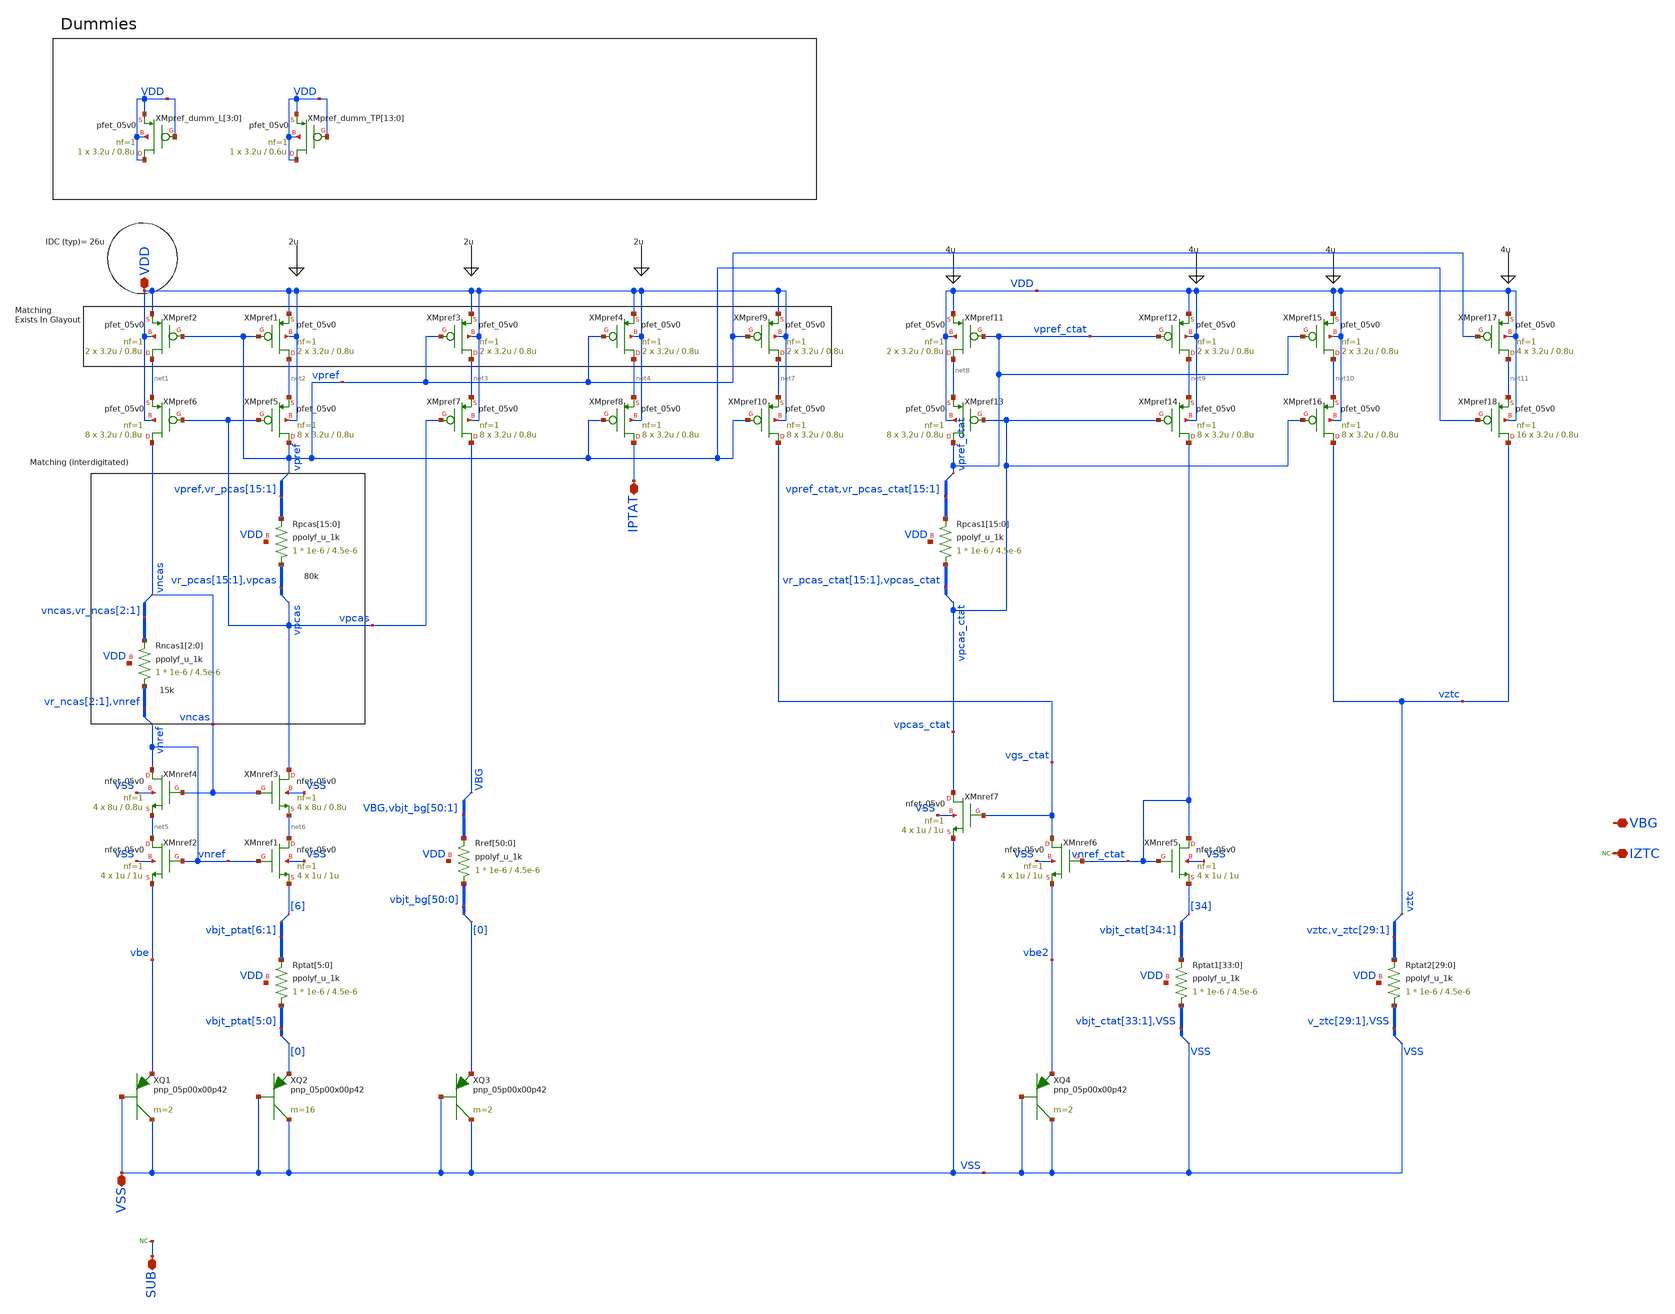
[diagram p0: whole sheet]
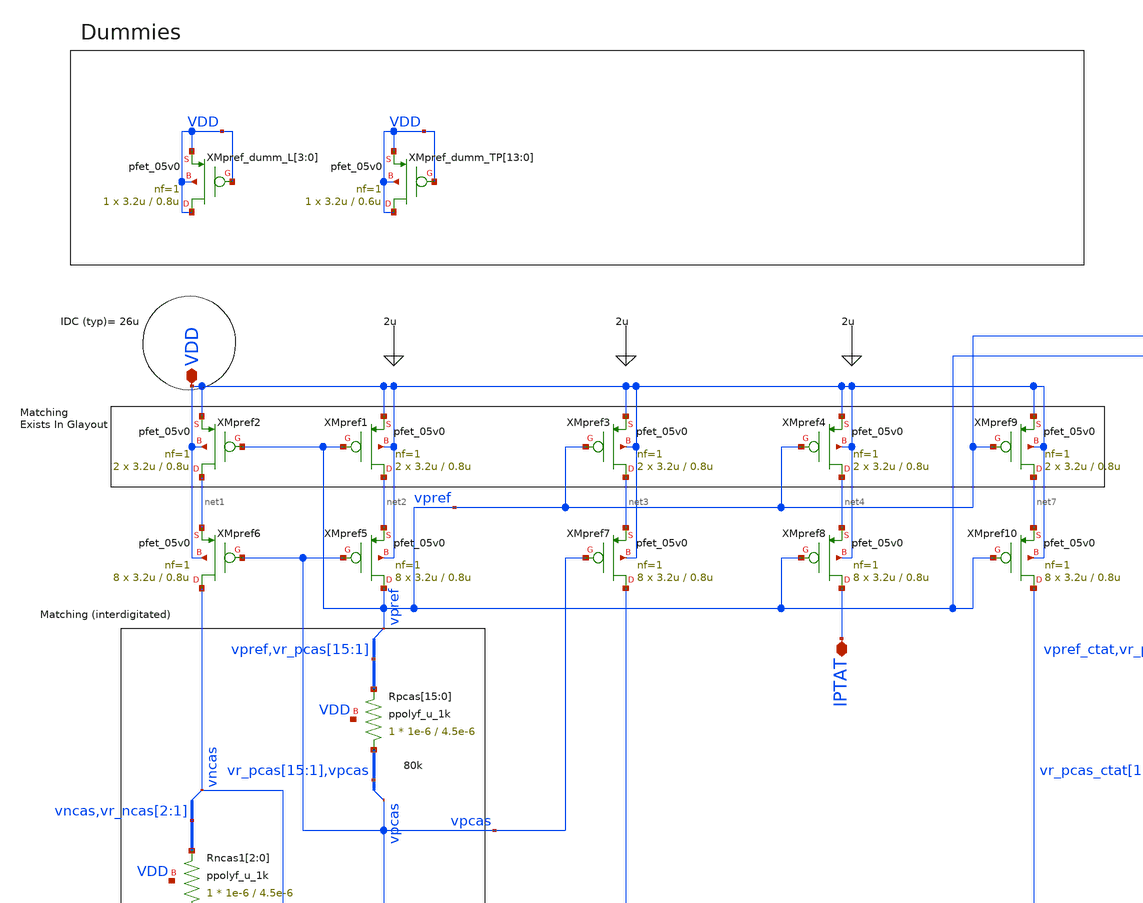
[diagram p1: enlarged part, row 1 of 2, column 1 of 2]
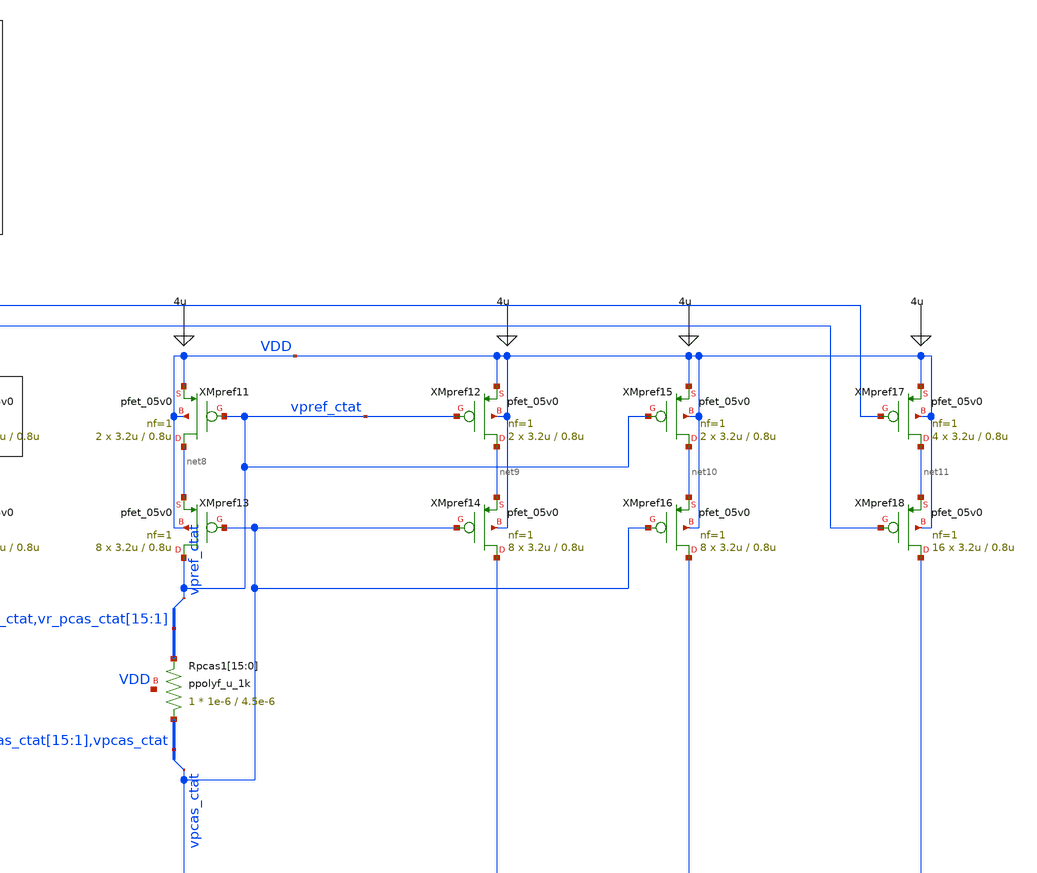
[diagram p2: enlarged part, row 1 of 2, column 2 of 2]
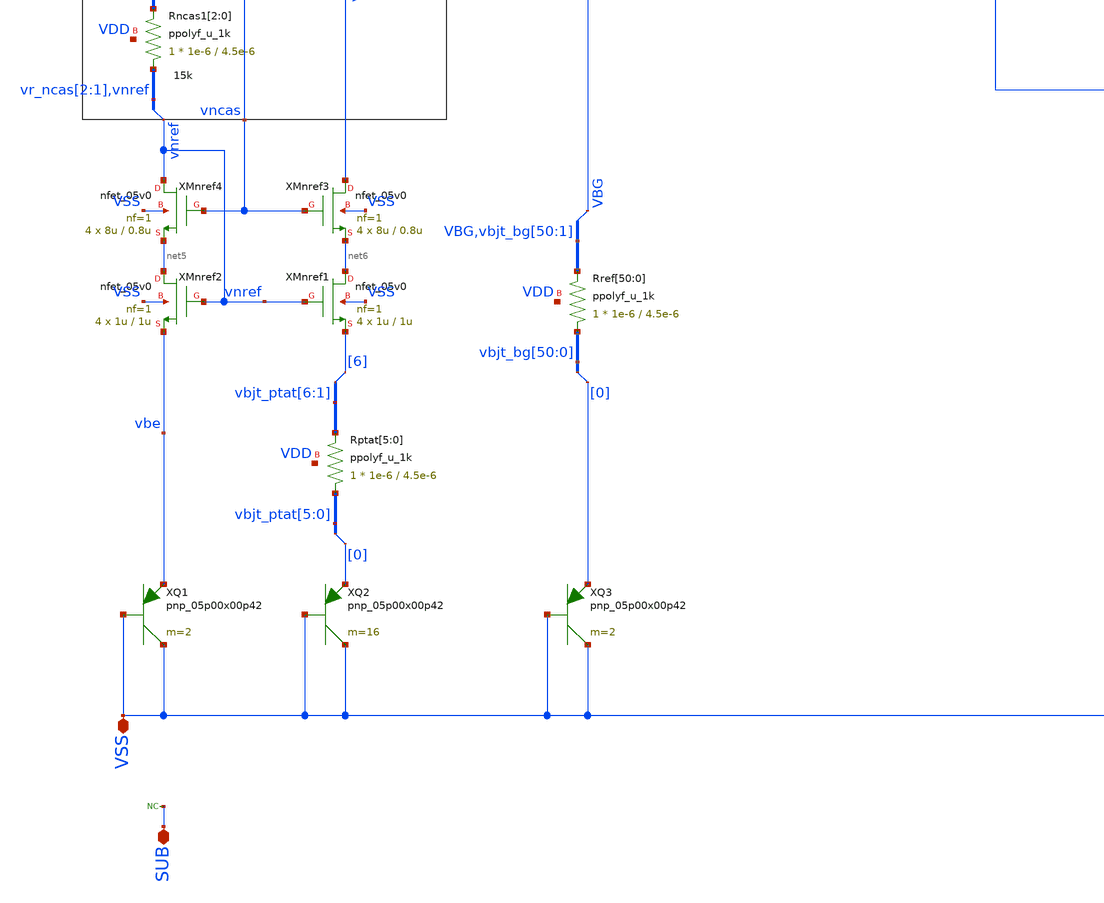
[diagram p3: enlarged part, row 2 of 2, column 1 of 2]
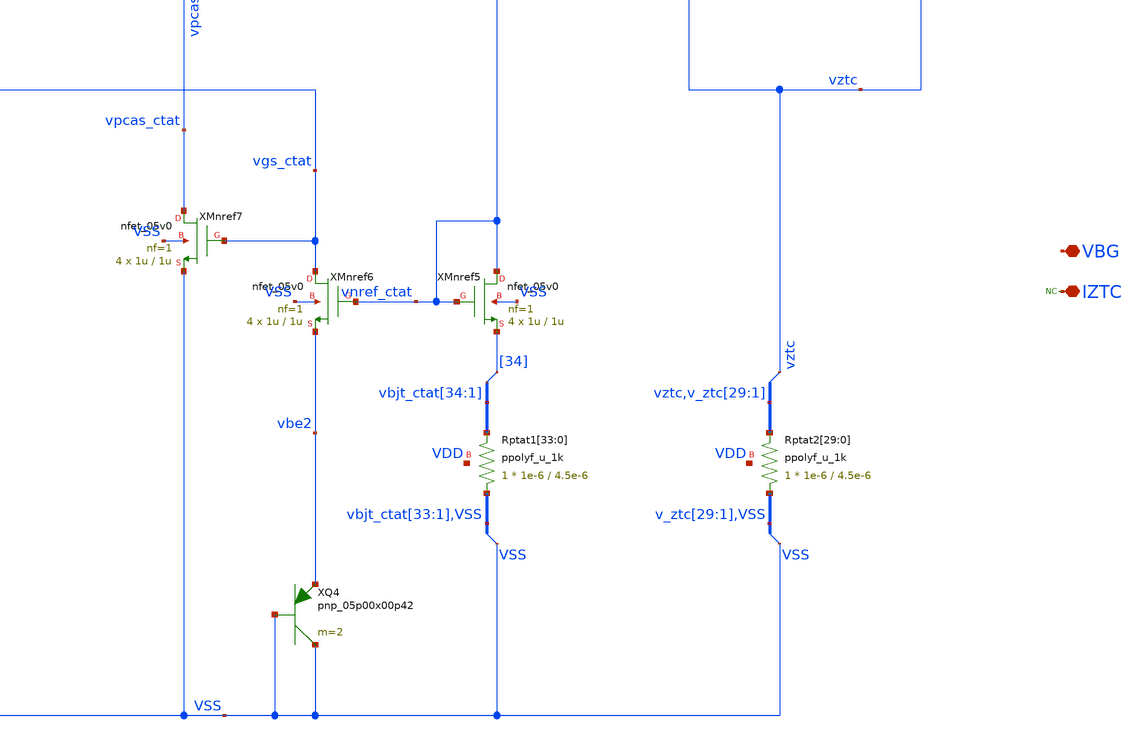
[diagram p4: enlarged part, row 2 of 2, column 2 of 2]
** sch_path: designs/libs/core_bandgap/bandgap/bandgap_no_opamp.sch
**.subckt bandgap_no_opamp VDD VSS SUB VBG IPTAT IZTC
*.iopin VDD
*.iopin VSS
*.iopin SUB
*.iopin VBG
*.iopin IPTAT
*.iopin IZTC
* noconn SUB
XQ1 VSS VSS vbe pnp_05p00x00p42 m=2 par=2
XQ2 VSS VSS vbjt_ptat[0] pnp_05p00x00p42 m=16 par=16
XMpref1 net2 vpref VDD VDD pfet_05v0 L=0.8u W=3.2u nf=1 ad='int((nf+1)/2) * W/nf * 0.18u' as='int((nf+2)/2) * W/nf * 0.18u'
+ pd='2*int((nf+1)/2) * (W/nf + 0.18u)' ps='2*int((nf+2)/2) * (W/nf + 0.18u)' nrd='0.18u / W' nrs='0.18u / W'
+ sa=0 sb=0 sd=0 m=2
XMnref1 net6 vnref vbjt_ptat[6] VSS nfet_05v0 L=1u W=1u nf=1 ad='int((nf+1)/2) * W/nf * 0.18u' as='int((nf+2)/2) * W/nf * 0.18u'
+ pd='2*int((nf+1)/2) * (W/nf + 0.18u)' ps='2*int((nf+2)/2) * (W/nf + 0.18u)' nrd='0.18u / W' nrs='0.18u / W'
+ sa=0 sb=0 sd=0 m=4
XMnref2 net5 vnref vbe VSS nfet_05v0 L=1u W=1u nf=1 ad='int((nf+1)/2) * W/nf * 0.18u' as='int((nf+2)/2) * W/nf * 0.18u'
+ pd='2*int((nf+1)/2) * (W/nf + 0.18u)' ps='2*int((nf+2)/2) * (W/nf + 0.18u)' nrd='0.18u / W' nrs='0.18u / W'
+ sa=0 sb=0 sd=0 m=4
XMpref2 net1 vpref VDD VDD pfet_05v0 L=0.8u W=3.2u nf=1 ad='int((nf+1)/2) * W/nf * 0.18u' as='int((nf+2)/2) * W/nf * 0.18u'
+ pd='2*int((nf+1)/2) * (W/nf + 0.18u)' ps='2*int((nf+2)/2) * (W/nf + 0.18u)' nrd='0.18u / W' nrs='0.18u / W'
+ sa=0 sb=0 sd=0 m=2
XRptat[5] vbjt_ptat[5] vbjt_ptat[6] VDD ppolyf_u_1k r_width=1e-6 r_length=4.5e-6 m=1
XRptat[4] vbjt_ptat[4] vbjt_ptat[5] VDD ppolyf_u_1k r_width=1e-6 r_length=4.5e-6 m=1
XRptat[3] vbjt_ptat[3] vbjt_ptat[4] VDD ppolyf_u_1k r_width=1e-6 r_length=4.5e-6 m=1
XRptat[2] vbjt_ptat[2] vbjt_ptat[3] VDD ppolyf_u_1k r_width=1e-6 r_length=4.5e-6 m=1
XRptat[1] vbjt_ptat[1] vbjt_ptat[2] VDD ppolyf_u_1k r_width=1e-6 r_length=4.5e-6 m=1
XRptat[0] vbjt_ptat[0] vbjt_ptat[1] VDD ppolyf_u_1k r_width=1e-6 r_length=4.5e-6 m=1
* tap: vbjt_ptat[5:0] --> vbjt_ptat[0]
* tap: vbjt_ptat[6:1] --> vbjt_ptat[6]
XQ3 VSS VSS vbjt_bg[0] pnp_05p00x00p42 m=2 par=2
XMpref3 net3 vpref VDD VDD pfet_05v0 L=0.8u W=3.2u nf=1 ad='int((nf+1)/2) * W/nf * 0.18u' as='int((nf+2)/2) * W/nf * 0.18u'
+ pd='2*int((nf+1)/2) * (W/nf + 0.18u)' ps='2*int((nf+2)/2) * (W/nf + 0.18u)' nrd='0.18u / W' nrs='0.18u / W'
+ sa=0 sb=0 sd=0 m=2
XRref[50] vbjt_bg[50] VBG VDD ppolyf_u_1k r_width=1e-6 r_length=4.5e-6 m=1
XRref[49] vbjt_bg[49] vbjt_bg[50] VDD ppolyf_u_1k r_width=1e-6 r_length=4.5e-6 m=1
XRref[48] vbjt_bg[48] vbjt_bg[49] VDD ppolyf_u_1k r_width=1e-6 r_length=4.5e-6 m=1
XRref[47] vbjt_bg[47] vbjt_bg[48] VDD ppolyf_u_1k r_width=1e-6 r_length=4.5e-6 m=1
XRref[46] vbjt_bg[46] vbjt_bg[47] VDD ppolyf_u_1k r_width=1e-6 r_length=4.5e-6 m=1
XRref[45] vbjt_bg[45] vbjt_bg[46] VDD ppolyf_u_1k r_width=1e-6 r_length=4.5e-6 m=1
XRref[44] vbjt_bg[44] vbjt_bg[45] VDD ppolyf_u_1k r_width=1e-6 r_length=4.5e-6 m=1
XRref[43] vbjt_bg[43] vbjt_bg[44] VDD ppolyf_u_1k r_width=1e-6 r_length=4.5e-6 m=1
XRref[42] vbjt_bg[42] vbjt_bg[43] VDD ppolyf_u_1k r_width=1e-6 r_length=4.5e-6 m=1
XRref[41] vbjt_bg[41] vbjt_bg[42] VDD ppolyf_u_1k r_width=1e-6 r_length=4.5e-6 m=1
XRref[40] vbjt_bg[40] vbjt_bg[41] VDD ppolyf_u_1k r_width=1e-6 r_length=4.5e-6 m=1
XRref[39] vbjt_bg[39] vbjt_bg[40] VDD ppolyf_u_1k r_width=1e-6 r_length=4.5e-6 m=1
XRref[38] vbjt_bg[38] vbjt_bg[39] VDD ppolyf_u_1k r_width=1e-6 r_length=4.5e-6 m=1
XRref[37] vbjt_bg[37] vbjt_bg[38] VDD ppolyf_u_1k r_width=1e-6 r_length=4.5e-6 m=1
XRref[36] vbjt_bg[36] vbjt_bg[37] VDD ppolyf_u_1k r_width=1e-6 r_length=4.5e-6 m=1
XRref[35] vbjt_bg[35] vbjt_bg[36] VDD ppolyf_u_1k r_width=1e-6 r_length=4.5e-6 m=1
XRref[34] vbjt_bg[34] vbjt_bg[35] VDD ppolyf_u_1k r_width=1e-6 r_length=4.5e-6 m=1
XRref[33] vbjt_bg[33] vbjt_bg[34] VDD ppolyf_u_1k r_width=1e-6 r_length=4.5e-6 m=1
XRref[32] vbjt_bg[32] vbjt_bg[33] VDD ppolyf_u_1k r_width=1e-6 r_length=4.5e-6 m=1
XRref[31] vbjt_bg[31] vbjt_bg[32] VDD ppolyf_u_1k r_width=1e-6 r_length=4.5e-6 m=1
XRref[30] vbjt_bg[30] vbjt_bg[31] VDD ppolyf_u_1k r_width=1e-6 r_length=4.5e-6 m=1
XRref[29] vbjt_bg[29] vbjt_bg[30] VDD ppolyf_u_1k r_width=1e-6 r_length=4.5e-6 m=1
XRref[28] vbjt_bg[28] vbjt_bg[29] VDD ppolyf_u_1k r_width=1e-6 r_length=4.5e-6 m=1
XRref[27] vbjt_bg[27] vbjt_bg[28] VDD ppolyf_u_1k r_width=1e-6 r_length=4.5e-6 m=1
XRref[26] vbjt_bg[26] vbjt_bg[27] VDD ppolyf_u_1k r_width=1e-6 r_length=4.5e-6 m=1
XRref[25] vbjt_bg[25] vbjt_bg[26] VDD ppolyf_u_1k r_width=1e-6 r_length=4.5e-6 m=1
XRref[24] vbjt_bg[24] vbjt_bg[25] VDD ppolyf_u_1k r_width=1e-6 r_length=4.5e-6 m=1
XRref[23] vbjt_bg[23] vbjt_bg[24] VDD ppolyf_u_1k r_width=1e-6 r_length=4.5e-6 m=1
XRref[22] vbjt_bg[22] vbjt_bg[23] VDD ppolyf_u_1k r_width=1e-6 r_length=4.5e-6 m=1
XRref[21] vbjt_bg[21] vbjt_bg[22] VDD ppolyf_u_1k r_width=1e-6 r_length=4.5e-6 m=1
XRref[20] vbjt_bg[20] vbjt_bg[21] VDD ppolyf_u_1k r_width=1e-6 r_length=4.5e-6 m=1
XRref[19] vbjt_bg[19] vbjt_bg[20] VDD ppolyf_u_1k r_width=1e-6 r_length=4.5e-6 m=1
XRref[18] vbjt_bg[18] vbjt_bg[19] VDD ppolyf_u_1k r_width=1e-6 r_length=4.5e-6 m=1
XRref[17] vbjt_bg[17] vbjt_bg[18] VDD ppolyf_u_1k r_width=1e-6 r_length=4.5e-6 m=1
XRref[16] vbjt_bg[16] vbjt_bg[17] VDD ppolyf_u_1k r_width=1e-6 r_length=4.5e-6 m=1
XRref[15] vbjt_bg[15] vbjt_bg[16] VDD ppolyf_u_1k r_width=1e-6 r_length=4.5e-6 m=1
XRref[14] vbjt_bg[14] vbjt_bg[15] VDD ppolyf_u_1k r_width=1e-6 r_length=4.5e-6 m=1
XRref[13] vbjt_bg[13] vbjt_bg[14] VDD ppolyf_u_1k r_width=1e-6 r_length=4.5e-6 m=1
XRref[12] vbjt_bg[12] vbjt_bg[13] VDD ppolyf_u_1k r_width=1e-6 r_length=4.5e-6 m=1
XRref[11] vbjt_bg[11] vbjt_bg[12] VDD ppolyf_u_1k r_width=1e-6 r_length=4.5e-6 m=1
XRref[10] vbjt_bg[10] vbjt_bg[11] VDD ppolyf_u_1k r_width=1e-6 r_length=4.5e-6 m=1
XRref[9] vbjt_bg[9] vbjt_bg[10] VDD ppolyf_u_1k r_width=1e-6 r_length=4.5e-6 m=1
XRref[8] vbjt_bg[8] vbjt_bg[9] VDD ppolyf_u_1k r_width=1e-6 r_length=4.5e-6 m=1
XRref[7] vbjt_bg[7] vbjt_bg[8] VDD ppolyf_u_1k r_width=1e-6 r_length=4.5e-6 m=1
XRref[6] vbjt_bg[6] vbjt_bg[7] VDD ppolyf_u_1k r_width=1e-6 r_length=4.5e-6 m=1
XRref[5] vbjt_bg[5] vbjt_bg[6] VDD ppolyf_u_1k r_width=1e-6 r_length=4.5e-6 m=1
XRref[4] vbjt_bg[4] vbjt_bg[5] VDD ppolyf_u_1k r_width=1e-6 r_length=4.5e-6 m=1
XRref[3] vbjt_bg[3] vbjt_bg[4] VDD ppolyf_u_1k r_width=1e-6 r_length=4.5e-6 m=1
XRref[2] vbjt_bg[2] vbjt_bg[3] VDD ppolyf_u_1k r_width=1e-6 r_length=4.5e-6 m=1
XRref[1] vbjt_bg[1] vbjt_bg[2] VDD ppolyf_u_1k r_width=1e-6 r_length=4.5e-6 m=1
XRref[0] vbjt_bg[0] vbjt_bg[1] VDD ppolyf_u_1k r_width=1e-6 r_length=4.5e-6 m=1
* tap: vbjt_bg[50:0] --> vbjt_bg[0]
XMpref4 net4 vpref VDD VDD pfet_05v0 L=0.8u W=3.2u nf=1 ad='int((nf+1)/2) * W/nf * 0.18u' as='int((nf+2)/2) * W/nf * 0.18u'
+ pd='2*int((nf+1)/2) * (W/nf + 0.18u)' ps='2*int((nf+2)/2) * (W/nf + 0.18u)' nrd='0.18u / W' nrs='0.18u / W'
+ sa=0 sb=0 sd=0 m=2
* noconn IZTC
XMpref5 vpref vpcas net2 VDD pfet_05v0 L=0.8u W=3.2u nf=1 ad='int((nf+1)/2) * W/nf * 0.18u' as='int((nf+2)/2) * W/nf * 0.18u'
+ pd='2*int((nf+1)/2) * (W/nf + 0.18u)' ps='2*int((nf+2)/2) * (W/nf + 0.18u)' nrd='0.18u / W' nrs='0.18u / W'
+ sa=0 sb=0 sd=0 m=8
XMpref6 vncas vpcas net1 VDD pfet_05v0 L=0.8u W=3.2u nf=1 ad='int((nf+1)/2) * W/nf * 0.18u' as='int((nf+2)/2) * W/nf * 0.18u'
+ pd='2*int((nf+1)/2) * (W/nf + 0.18u)' ps='2*int((nf+2)/2) * (W/nf + 0.18u)' nrd='0.18u / W' nrs='0.18u / W'
+ sa=0 sb=0 sd=0 m=8
XMpref7 VBG vpcas net3 VDD pfet_05v0 L=0.8u W=3.2u nf=1 ad='int((nf+1)/2) * W/nf * 0.18u' as='int((nf+2)/2) * W/nf * 0.18u'
+ pd='2*int((nf+1)/2) * (W/nf + 0.18u)' ps='2*int((nf+2)/2) * (W/nf + 0.18u)' nrd='0.18u / W' nrs='0.18u / W'
+ sa=0 sb=0 sd=0 m=8
XMpref8 IPTAT vpref net4 VDD pfet_05v0 L=0.8u W=3.2u nf=1 ad='int((nf+1)/2) * W/nf * 0.18u' as='int((nf+2)/2) * W/nf * 0.18u'
+ pd='2*int((nf+1)/2) * (W/nf + 0.18u)' ps='2*int((nf+2)/2) * (W/nf + 0.18u)' nrd='0.18u / W' nrs='0.18u / W'
+ sa=0 sb=0 sd=0 m=8
XRpcas[15] vr_pcas[15] vpref VDD ppolyf_u_1k r_width=1e-6 r_length=4.5e-6 m=1
XRpcas[14] vr_pcas[14] vr_pcas[15] VDD ppolyf_u_1k r_width=1e-6 r_length=4.5e-6 m=1
XRpcas[13] vr_pcas[13] vr_pcas[14] VDD ppolyf_u_1k r_width=1e-6 r_length=4.5e-6 m=1
XRpcas[12] vr_pcas[12] vr_pcas[13] VDD ppolyf_u_1k r_width=1e-6 r_length=4.5e-6 m=1
XRpcas[11] vr_pcas[11] vr_pcas[12] VDD ppolyf_u_1k r_width=1e-6 r_length=4.5e-6 m=1
XRpcas[10] vr_pcas[10] vr_pcas[11] VDD ppolyf_u_1k r_width=1e-6 r_length=4.5e-6 m=1
XRpcas[9] vr_pcas[9] vr_pcas[10] VDD ppolyf_u_1k r_width=1e-6 r_length=4.5e-6 m=1
XRpcas[8] vr_pcas[8] vr_pcas[9] VDD ppolyf_u_1k r_width=1e-6 r_length=4.5e-6 m=1
XRpcas[7] vr_pcas[7] vr_pcas[8] VDD ppolyf_u_1k r_width=1e-6 r_length=4.5e-6 m=1
XRpcas[6] vr_pcas[6] vr_pcas[7] VDD ppolyf_u_1k r_width=1e-6 r_length=4.5e-6 m=1
XRpcas[5] vr_pcas[5] vr_pcas[6] VDD ppolyf_u_1k r_width=1e-6 r_length=4.5e-6 m=1
XRpcas[4] vr_pcas[4] vr_pcas[5] VDD ppolyf_u_1k r_width=1e-6 r_length=4.5e-6 m=1
XRpcas[3] vr_pcas[3] vr_pcas[4] VDD ppolyf_u_1k r_width=1e-6 r_length=4.5e-6 m=1
XRpcas[2] vr_pcas[2] vr_pcas[3] VDD ppolyf_u_1k r_width=1e-6 r_length=4.5e-6 m=1
XRpcas[1] vr_pcas[1] vr_pcas[2] VDD ppolyf_u_1k r_width=1e-6 r_length=4.5e-6 m=1
XRpcas[0] vpcas vr_pcas[1] VDD ppolyf_u_1k r_width=1e-6 r_length=4.5e-6 m=1
XMnref3 vpcas vncas net6 VSS nfet_05v0 L=0.8u W=8u nf=1 ad='int((nf+1)/2) * W/nf * 0.18u' as='int((nf+2)/2) * W/nf * 0.18u'
+ pd='2*int((nf+1)/2) * (W/nf + 0.18u)' ps='2*int((nf+2)/2) * (W/nf + 0.18u)' nrd='0.18u / W' nrs='0.18u / W'
+ sa=0 sb=0 sd=0 m=4
XMnref4 vnref vncas net5 VSS nfet_05v0 L=0.8u W=8u nf=1 ad='int((nf+1)/2) * W/nf * 0.18u' as='int((nf+2)/2) * W/nf * 0.18u'
+ pd='2*int((nf+1)/2) * (W/nf + 0.18u)' ps='2*int((nf+2)/2) * (W/nf + 0.18u)' nrd='0.18u / W' nrs='0.18u / W'
+ sa=0 sb=0 sd=0 m=4
XRncas1[2] vr_ncas[2] vncas VDD ppolyf_u_1k r_width=1e-6 r_length=4.5e-6 m=1
XRncas1[1] vr_ncas[1] vr_ncas[2] VDD ppolyf_u_1k r_width=1e-6 r_length=4.5e-6 m=1
XRncas1[0] vnref vr_ncas[1] VDD ppolyf_u_1k r_width=1e-6 r_length=4.5e-6 m=1
XQ4 VSS VSS vbe2 pnp_05p00x00p42 m=2 par=2
XMnref5 vnref_ctat vnref_ctat vbjt_ctat[34] VSS nfet_05v0 L=1u W=1u nf=1 ad='int((nf+1)/2) * W/nf * 0.18u'
+ as='int((nf+2)/2) * W/nf * 0.18u' pd='2*int((nf+1)/2) * (W/nf + 0.18u)' ps='2*int((nf+2)/2) * (W/nf + 0.18u)'
+ nrd='0.18u / W' nrs='0.18u / W' sa=0 sb=0 sd=0 m=4
XMnref6 vgs_ctat vnref_ctat vbe2 VSS nfet_05v0 L=1u W=1u nf=1 ad='int((nf+1)/2) * W/nf * 0.18u' as='int((nf+2)/2) * W/nf * 0.18u'
+ pd='2*int((nf+1)/2) * (W/nf + 0.18u)' ps='2*int((nf+2)/2) * (W/nf + 0.18u)' nrd='0.18u / W' nrs='0.18u / W'
+ sa=0 sb=0 sd=0 m=4
XRptat1[33] vbjt_ctat[33] vbjt_ctat[34] VDD ppolyf_u_1k r_width=1e-6 r_length=4.5e-6 m=1
XRptat1[32] vbjt_ctat[32] vbjt_ctat[33] VDD ppolyf_u_1k r_width=1e-6 r_length=4.5e-6 m=1
XRptat1[31] vbjt_ctat[31] vbjt_ctat[32] VDD ppolyf_u_1k r_width=1e-6 r_length=4.5e-6 m=1
XRptat1[30] vbjt_ctat[30] vbjt_ctat[31] VDD ppolyf_u_1k r_width=1e-6 r_length=4.5e-6 m=1
XRptat1[29] vbjt_ctat[29] vbjt_ctat[30] VDD ppolyf_u_1k r_width=1e-6 r_length=4.5e-6 m=1
XRptat1[28] vbjt_ctat[28] vbjt_ctat[29] VDD ppolyf_u_1k r_width=1e-6 r_length=4.5e-6 m=1
XRptat1[27] vbjt_ctat[27] vbjt_ctat[28] VDD ppolyf_u_1k r_width=1e-6 r_length=4.5e-6 m=1
XRptat1[26] vbjt_ctat[26] vbjt_ctat[27] VDD ppolyf_u_1k r_width=1e-6 r_length=4.5e-6 m=1
XRptat1[25] vbjt_ctat[25] vbjt_ctat[26] VDD ppolyf_u_1k r_width=1e-6 r_length=4.5e-6 m=1
XRptat1[24] vbjt_ctat[24] vbjt_ctat[25] VDD ppolyf_u_1k r_width=1e-6 r_length=4.5e-6 m=1
XRptat1[23] vbjt_ctat[23] vbjt_ctat[24] VDD ppolyf_u_1k r_width=1e-6 r_length=4.5e-6 m=1
XRptat1[22] vbjt_ctat[22] vbjt_ctat[23] VDD ppolyf_u_1k r_width=1e-6 r_length=4.5e-6 m=1
XRptat1[21] vbjt_ctat[21] vbjt_ctat[22] VDD ppolyf_u_1k r_width=1e-6 r_length=4.5e-6 m=1
XRptat1[20] vbjt_ctat[20] vbjt_ctat[21] VDD ppolyf_u_1k r_width=1e-6 r_length=4.5e-6 m=1
XRptat1[19] vbjt_ctat[19] vbjt_ctat[20] VDD ppolyf_u_1k r_width=1e-6 r_length=4.5e-6 m=1
XRptat1[18] vbjt_ctat[18] vbjt_ctat[19] VDD ppolyf_u_1k r_width=1e-6 r_length=4.5e-6 m=1
XRptat1[17] vbjt_ctat[17] vbjt_ctat[18] VDD ppolyf_u_1k r_width=1e-6 r_length=4.5e-6 m=1
XRptat1[16] vbjt_ctat[16] vbjt_ctat[17] VDD ppolyf_u_1k r_width=1e-6 r_length=4.5e-6 m=1
XRptat1[15] vbjt_ctat[15] vbjt_ctat[16] VDD ppolyf_u_1k r_width=1e-6 r_length=4.5e-6 m=1
XRptat1[14] vbjt_ctat[14] vbjt_ctat[15] VDD ppolyf_u_1k r_width=1e-6 r_length=4.5e-6 m=1
XRptat1[13] vbjt_ctat[13] vbjt_ctat[14] VDD ppolyf_u_1k r_width=1e-6 r_length=4.5e-6 m=1
XRptat1[12] vbjt_ctat[12] vbjt_ctat[13] VDD ppolyf_u_1k r_width=1e-6 r_length=4.5e-6 m=1
XRptat1[11] vbjt_ctat[11] vbjt_ctat[12] VDD ppolyf_u_1k r_width=1e-6 r_length=4.5e-6 m=1
XRptat1[10] vbjt_ctat[10] vbjt_ctat[11] VDD ppolyf_u_1k r_width=1e-6 r_length=4.5e-6 m=1
XRptat1[9] vbjt_ctat[9] vbjt_ctat[10] VDD ppolyf_u_1k r_width=1e-6 r_length=4.5e-6 m=1
XRptat1[8] vbjt_ctat[8] vbjt_ctat[9] VDD ppolyf_u_1k r_width=1e-6 r_length=4.5e-6 m=1
XRptat1[7] vbjt_ctat[7] vbjt_ctat[8] VDD ppolyf_u_1k r_width=1e-6 r_length=4.5e-6 m=1
XRptat1[6] vbjt_ctat[6] vbjt_ctat[7] VDD ppolyf_u_1k r_width=1e-6 r_length=4.5e-6 m=1
XRptat1[5] vbjt_ctat[5] vbjt_ctat[6] VDD ppolyf_u_1k r_width=1e-6 r_length=4.5e-6 m=1
XRptat1[4] vbjt_ctat[4] vbjt_ctat[5] VDD ppolyf_u_1k r_width=1e-6 r_length=4.5e-6 m=1
XRptat1[3] vbjt_ctat[3] vbjt_ctat[4] VDD ppolyf_u_1k r_width=1e-6 r_length=4.5e-6 m=1
XRptat1[2] vbjt_ctat[2] vbjt_ctat[3] VDD ppolyf_u_1k r_width=1e-6 r_length=4.5e-6 m=1
XRptat1[1] vbjt_ctat[1] vbjt_ctat[2] VDD ppolyf_u_1k r_width=1e-6 r_length=4.5e-6 m=1
XRptat1[0] VSS vbjt_ctat[1] VDD ppolyf_u_1k r_width=1e-6 r_length=4.5e-6 m=1
* tap: vbjt_ctat[34:1] --> vbjt_ctat[34]
XMnref7 vpcas_ctat vgs_ctat VSS VSS nfet_05v0 L=1u W=1u nf=1 ad='int((nf+1)/2) * W/nf * 0.18u' as='int((nf+2)/2) * W/nf * 0.18u'
+ pd='2*int((nf+1)/2) * (W/nf + 0.18u)' ps='2*int((nf+2)/2) * (W/nf + 0.18u)' nrd='0.18u / W' nrs='0.18u / W'
+ sa=0 sb=0 sd=0 m=4
XMpref9 net7 vpref VDD VDD pfet_05v0 L=0.8u W=3.2u nf=1 ad='int((nf+1)/2) * W/nf * 0.18u' as='int((nf+2)/2) * W/nf * 0.18u'
+ pd='2*int((nf+1)/2) * (W/nf + 0.18u)' ps='2*int((nf+2)/2) * (W/nf + 0.18u)' nrd='0.18u / W' nrs='0.18u / W'
+ sa=0 sb=0 sd=0 m=2
XMpref10 vgs_ctat vpref net7 VDD pfet_05v0 L=0.8u W=3.2u nf=1 ad='int((nf+1)/2) * W/nf * 0.18u' as='int((nf+2)/2) * W/nf * 0.18u'
+ pd='2*int((nf+1)/2) * (W/nf + 0.18u)' ps='2*int((nf+2)/2) * (W/nf + 0.18u)' nrd='0.18u / W' nrs='0.18u / W'
+ sa=0 sb=0 sd=0 m=8
XMpref11 net8 vpref_ctat VDD VDD pfet_05v0 L=0.8u W=3.2u nf=1 ad='int((nf+1)/2) * W/nf * 0.18u' as='int((nf+2)/2) * W/nf * 0.18u'
+ pd='2*int((nf+1)/2) * (W/nf + 0.18u)' ps='2*int((nf+2)/2) * (W/nf + 0.18u)' nrd='0.18u / W' nrs='0.18u / W'
+ sa=0 sb=0 sd=0 m=2
XMpref12 net9 vpref_ctat VDD VDD pfet_05v0 L=0.8u W=3.2u nf=1 ad='int((nf+1)/2) * W/nf * 0.18u' as='int((nf+2)/2) * W/nf * 0.18u'
+ pd='2*int((nf+1)/2) * (W/nf + 0.18u)' ps='2*int((nf+2)/2) * (W/nf + 0.18u)' nrd='0.18u / W' nrs='0.18u / W'
+ sa=0 sb=0 sd=0 m=2
XRpcas1[15] vr_pcas_ctat[15] vpref_ctat VDD ppolyf_u_1k r_width=1e-6 r_length=4.5e-6 m=1
XRpcas1[14] vr_pcas_ctat[14] vr_pcas_ctat[15] VDD ppolyf_u_1k r_width=1e-6 r_length=4.5e-6 m=1
XRpcas1[13] vr_pcas_ctat[13] vr_pcas_ctat[14] VDD ppolyf_u_1k r_width=1e-6 r_length=4.5e-6 m=1
XRpcas1[12] vr_pcas_ctat[12] vr_pcas_ctat[13] VDD ppolyf_u_1k r_width=1e-6 r_length=4.5e-6 m=1
XRpcas1[11] vr_pcas_ctat[11] vr_pcas_ctat[12] VDD ppolyf_u_1k r_width=1e-6 r_length=4.5e-6 m=1
XRpcas1[10] vr_pcas_ctat[10] vr_pcas_ctat[11] VDD ppolyf_u_1k r_width=1e-6 r_length=4.5e-6 m=1
XRpcas1[9] vr_pcas_ctat[9] vr_pcas_ctat[10] VDD ppolyf_u_1k r_width=1e-6 r_length=4.5e-6 m=1
XRpcas1[8] vr_pcas_ctat[8] vr_pcas_ctat[9] VDD ppolyf_u_1k r_width=1e-6 r_length=4.5e-6 m=1
XRpcas1[7] vr_pcas_ctat[7] vr_pcas_ctat[8] VDD ppolyf_u_1k r_width=1e-6 r_length=4.5e-6 m=1
XRpcas1[6] vr_pcas_ctat[6] vr_pcas_ctat[7] VDD ppolyf_u_1k r_width=1e-6 r_length=4.5e-6 m=1
XRpcas1[5] vr_pcas_ctat[5] vr_pcas_ctat[6] VDD ppolyf_u_1k r_width=1e-6 r_length=4.5e-6 m=1
XRpcas1[4] vr_pcas_ctat[4] vr_pcas_ctat[5] VDD ppolyf_u_1k r_width=1e-6 r_length=4.5e-6 m=1
XRpcas1[3] vr_pcas_ctat[3] vr_pcas_ctat[4] VDD ppolyf_u_1k r_width=1e-6 r_length=4.5e-6 m=1
XRpcas1[2] vr_pcas_ctat[2] vr_pcas_ctat[3] VDD ppolyf_u_1k r_width=1e-6 r_length=4.5e-6 m=1
XRpcas1[1] vr_pcas_ctat[1] vr_pcas_ctat[2] VDD ppolyf_u_1k r_width=1e-6 r_length=4.5e-6 m=1
XRpcas1[0] vpcas_ctat vr_pcas_ctat[1] VDD ppolyf_u_1k r_width=1e-6 r_length=4.5e-6 m=1
XMpref13 vpref_ctat vpcas_ctat net8 VDD pfet_05v0 L=0.8u W=3.2u nf=1 ad='int((nf+1)/2) * W/nf * 0.18u'
+ as='int((nf+2)/2) * W/nf * 0.18u' pd='2*int((nf+1)/2) * (W/nf + 0.18u)' ps='2*int((nf+2)/2) * (W/nf + 0.18u)'
+ nrd='0.18u / W' nrs='0.18u / W' sa=0 sb=0 sd=0 m=8
XMpref14 vnref_ctat vpcas_ctat net9 VDD pfet_05v0 L=0.8u W=3.2u nf=1 ad='int((nf+1)/2) * W/nf * 0.18u'
+ as='int((nf+2)/2) * W/nf * 0.18u' pd='2*int((nf+1)/2) * (W/nf + 0.18u)' ps='2*int((nf+2)/2) * (W/nf + 0.18u)'
+ nrd='0.18u / W' nrs='0.18u / W' sa=0 sb=0 sd=0 m=8
XMpref15 net10 vpref_ctat VDD VDD pfet_05v0 L=0.8u W=3.2u nf=1 ad='int((nf+1)/2) * W/nf * 0.18u' as='int((nf+2)/2) * W/nf * 0.18u'
+ pd='2*int((nf+1)/2) * (W/nf + 0.18u)' ps='2*int((nf+2)/2) * (W/nf + 0.18u)' nrd='0.18u / W' nrs='0.18u / W'
+ sa=0 sb=0 sd=0 m=2
XMpref16 vztc vpcas_ctat net10 VDD pfet_05v0 L=0.8u W=3.2u nf=1 ad='int((nf+1)/2) * W/nf * 0.18u' as='int((nf+2)/2) * W/nf * 0.18u'
+ pd='2*int((nf+1)/2) * (W/nf + 0.18u)' ps='2*int((nf+2)/2) * (W/nf + 0.18u)' nrd='0.18u / W' nrs='0.18u / W'
+ sa=0 sb=0 sd=0 m=8
XRptat2[29] v_ztc[29] vztc VDD ppolyf_u_1k r_width=1e-6 r_length=4.5e-6 m=1
XRptat2[28] v_ztc[28] v_ztc[29] VDD ppolyf_u_1k r_width=1e-6 r_length=4.5e-6 m=1
XRptat2[27] v_ztc[27] v_ztc[28] VDD ppolyf_u_1k r_width=1e-6 r_length=4.5e-6 m=1
XRptat2[26] v_ztc[26] v_ztc[27] VDD ppolyf_u_1k r_width=1e-6 r_length=4.5e-6 m=1
XRptat2[25] v_ztc[25] v_ztc[26] VDD ppolyf_u_1k r_width=1e-6 r_length=4.5e-6 m=1
XRptat2[24] v_ztc[24] v_ztc[25] VDD ppolyf_u_1k r_width=1e-6 r_length=4.5e-6 m=1
XRptat2[23] v_ztc[23] v_ztc[24] VDD ppolyf_u_1k r_width=1e-6 r_length=4.5e-6 m=1
XRptat2[22] v_ztc[22] v_ztc[23] VDD ppolyf_u_1k r_width=1e-6 r_length=4.5e-6 m=1
XRptat2[21] v_ztc[21] v_ztc[22] VDD ppolyf_u_1k r_width=1e-6 r_length=4.5e-6 m=1
XRptat2[20] v_ztc[20] v_ztc[21] VDD ppolyf_u_1k r_width=1e-6 r_length=4.5e-6 m=1
XRptat2[19] v_ztc[19] v_ztc[20] VDD ppolyf_u_1k r_width=1e-6 r_length=4.5e-6 m=1
XRptat2[18] v_ztc[18] v_ztc[19] VDD ppolyf_u_1k r_width=1e-6 r_length=4.5e-6 m=1
XRptat2[17] v_ztc[17] v_ztc[18] VDD ppolyf_u_1k r_width=1e-6 r_length=4.5e-6 m=1
XRptat2[16] v_ztc[16] v_ztc[17] VDD ppolyf_u_1k r_width=1e-6 r_length=4.5e-6 m=1
XRptat2[15] v_ztc[15] v_ztc[16] VDD ppolyf_u_1k r_width=1e-6 r_length=4.5e-6 m=1
XRptat2[14] v_ztc[14] v_ztc[15] VDD ppolyf_u_1k r_width=1e-6 r_length=4.5e-6 m=1
XRptat2[13] v_ztc[13] v_ztc[14] VDD ppolyf_u_1k r_width=1e-6 r_length=4.5e-6 m=1
XRptat2[12] v_ztc[12] v_ztc[13] VDD ppolyf_u_1k r_width=1e-6 r_length=4.5e-6 m=1
XRptat2[11] v_ztc[11] v_ztc[12] VDD ppolyf_u_1k r_width=1e-6 r_length=4.5e-6 m=1
XRptat2[10] v_ztc[10] v_ztc[11] VDD ppolyf_u_1k r_width=1e-6 r_length=4.5e-6 m=1
XRptat2[9] v_ztc[9] v_ztc[10] VDD ppolyf_u_1k r_width=1e-6 r_length=4.5e-6 m=1
XRptat2[8] v_ztc[8] v_ztc[9] VDD ppolyf_u_1k r_width=1e-6 r_length=4.5e-6 m=1
XRptat2[7] v_ztc[7] v_ztc[8] VDD ppolyf_u_1k r_width=1e-6 r_length=4.5e-6 m=1
XRptat2[6] v_ztc[6] v_ztc[7] VDD ppolyf_u_1k r_width=1e-6 r_length=4.5e-6 m=1
XRptat2[5] v_ztc[5] v_ztc[6] VDD ppolyf_u_1k r_width=1e-6 r_length=4.5e-6 m=1
XRptat2[4] v_ztc[4] v_ztc[5] VDD ppolyf_u_1k r_width=1e-6 r_length=4.5e-6 m=1
XRptat2[3] v_ztc[3] v_ztc[4] VDD ppolyf_u_1k r_width=1e-6 r_length=4.5e-6 m=1
XRptat2[2] v_ztc[2] v_ztc[3] VDD ppolyf_u_1k r_width=1e-6 r_length=4.5e-6 m=1
XRptat2[1] v_ztc[1] v_ztc[2] VDD ppolyf_u_1k r_width=1e-6 r_length=4.5e-6 m=1
XRptat2[0] VSS v_ztc[1] VDD ppolyf_u_1k r_width=1e-6 r_length=4.5e-6 m=1
XMpref17 net11 vpref VDD VDD pfet_05v0 L=0.8u W=3.2u nf=1 ad='int((nf+1)/2) * W/nf * 0.18u' as='int((nf+2)/2) * W/nf * 0.18u'
+ pd='2*int((nf+1)/2) * (W/nf + 0.18u)' ps='2*int((nf+2)/2) * (W/nf + 0.18u)' nrd='0.18u / W' nrs='0.18u / W'
+ sa=0 sb=0 sd=0 m=4
XMpref18 vztc vpref net11 VDD pfet_05v0 L=0.8u W=3.2u nf=1 ad='int((nf+1)/2) * W/nf * 0.18u' as='int((nf+2)/2) * W/nf * 0.18u'
+ pd='2*int((nf+1)/2) * (W/nf + 0.18u)' ps='2*int((nf+2)/2) * (W/nf + 0.18u)' nrd='0.18u / W' nrs='0.18u / W'
+ sa=0 sb=0 sd=0 m=16
XMpref_dumm_L[3] VDD VDD VDD VDD pfet_05v0 L=0.8u W=3.2u nf=1 ad='int((nf+1)/2) * W/nf * 0.18u' as='int((nf+2)/2) * W/nf * 0.18u'
+ pd='2*int((nf+1)/2) * (W/nf + 0.18u)' ps='2*int((nf+2)/2) * (W/nf + 0.18u)' nrd='0.18u / W' nrs='0.18u / W'
+ sa=0 sb=0 sd=0 m=1
XMpref_dumm_L[2] VDD VDD VDD VDD pfet_05v0 L=0.8u W=3.2u nf=1 ad='int((nf+1)/2) * W/nf * 0.18u' as='int((nf+2)/2) * W/nf * 0.18u'
+ pd='2*int((nf+1)/2) * (W/nf + 0.18u)' ps='2*int((nf+2)/2) * (W/nf + 0.18u)' nrd='0.18u / W' nrs='0.18u / W'
+ sa=0 sb=0 sd=0 m=1
XMpref_dumm_L[1] VDD VDD VDD VDD pfet_05v0 L=0.8u W=3.2u nf=1 ad='int((nf+1)/2) * W/nf * 0.18u' as='int((nf+2)/2) * W/nf * 0.18u'
+ pd='2*int((nf+1)/2) * (W/nf + 0.18u)' ps='2*int((nf+2)/2) * (W/nf + 0.18u)' nrd='0.18u / W' nrs='0.18u / W'
+ sa=0 sb=0 sd=0 m=1
XMpref_dumm_L[0] VDD VDD VDD VDD pfet_05v0 L=0.8u W=3.2u nf=1 ad='int((nf+1)/2) * W/nf * 0.18u' as='int((nf+2)/2) * W/nf * 0.18u'
+ pd='2*int((nf+1)/2) * (W/nf + 0.18u)' ps='2*int((nf+2)/2) * (W/nf + 0.18u)' nrd='0.18u / W' nrs='0.18u / W'
+ sa=0 sb=0 sd=0 m=1
XMpref_dumm_TP[13] VDD VDD VDD VDD pfet_05v0 L=0.6u W=3.2u nf=1 ad='int((nf+1)/2) * W/nf * 0.18u' as='int((nf+2)/2) * W/nf * 0.18u'
+ pd='2*int((nf+1)/2) * (W/nf + 0.18u)' ps='2*int((nf+2)/2) * (W/nf + 0.18u)' nrd='0.18u / W' nrs='0.18u / W'
+ sa=0 sb=0 sd=0 m=1
XMpref_dumm_TP[12] VDD VDD VDD VDD pfet_05v0 L=0.6u W=3.2u nf=1 ad='int((nf+1)/2) * W/nf * 0.18u' as='int((nf+2)/2) * W/nf * 0.18u'
+ pd='2*int((nf+1)/2) * (W/nf + 0.18u)' ps='2*int((nf+2)/2) * (W/nf + 0.18u)' nrd='0.18u / W' nrs='0.18u / W'
+ sa=0 sb=0 sd=0 m=1
XMpref_dumm_TP[11] VDD VDD VDD VDD pfet_05v0 L=0.6u W=3.2u nf=1 ad='int((nf+1)/2) * W/nf * 0.18u' as='int((nf+2)/2) * W/nf * 0.18u'
+ pd='2*int((nf+1)/2) * (W/nf + 0.18u)' ps='2*int((nf+2)/2) * (W/nf + 0.18u)' nrd='0.18u / W' nrs='0.18u / W'
+ sa=0 sb=0 sd=0 m=1
XMpref_dumm_TP[10] VDD VDD VDD VDD pfet_05v0 L=0.6u W=3.2u nf=1 ad='int((nf+1)/2) * W/nf * 0.18u' as='int((nf+2)/2) * W/nf * 0.18u'
+ pd='2*int((nf+1)/2) * (W/nf + 0.18u)' ps='2*int((nf+2)/2) * (W/nf + 0.18u)' nrd='0.18u / W' nrs='0.18u / W'
+ sa=0 sb=0 sd=0 m=1
XMpref_dumm_TP[9] VDD VDD VDD VDD pfet_05v0 L=0.6u W=3.2u nf=1 ad='int((nf+1)/2) * W/nf * 0.18u' as='int((nf+2)/2) * W/nf * 0.18u'
+ pd='2*int((nf+1)/2) * (W/nf + 0.18u)' ps='2*int((nf+2)/2) * (W/nf + 0.18u)' nrd='0.18u / W' nrs='0.18u / W'
+ sa=0 sb=0 sd=0 m=1
XMpref_dumm_TP[8] VDD VDD VDD VDD pfet_05v0 L=0.6u W=3.2u nf=1 ad='int((nf+1)/2) * W/nf * 0.18u' as='int((nf+2)/2) * W/nf * 0.18u'
+ pd='2*int((nf+1)/2) * (W/nf + 0.18u)' ps='2*int((nf+2)/2) * (W/nf + 0.18u)' nrd='0.18u / W' nrs='0.18u / W'
+ sa=0 sb=0 sd=0 m=1
XMpref_dumm_TP[7] VDD VDD VDD VDD pfet_05v0 L=0.6u W=3.2u nf=1 ad='int((nf+1)/2) * W/nf * 0.18u' as='int((nf+2)/2) * W/nf * 0.18u'
+ pd='2*int((nf+1)/2) * (W/nf + 0.18u)' ps='2*int((nf+2)/2) * (W/nf + 0.18u)' nrd='0.18u / W' nrs='0.18u / W'
+ sa=0 sb=0 sd=0 m=1
XMpref_dumm_TP[6] VDD VDD VDD VDD pfet_05v0 L=0.6u W=3.2u nf=1 ad='int((nf+1)/2) * W/nf * 0.18u' as='int((nf+2)/2) * W/nf * 0.18u'
+ pd='2*int((nf+1)/2) * (W/nf + 0.18u)' ps='2*int((nf+2)/2) * (W/nf + 0.18u)' nrd='0.18u / W' nrs='0.18u / W'
+ sa=0 sb=0 sd=0 m=1
XMpref_dumm_TP[5] VDD VDD VDD VDD pfet_05v0 L=0.6u W=3.2u nf=1 ad='int((nf+1)/2) * W/nf * 0.18u' as='int((nf+2)/2) * W/nf * 0.18u'
+ pd='2*int((nf+1)/2) * (W/nf + 0.18u)' ps='2*int((nf+2)/2) * (W/nf + 0.18u)' nrd='0.18u / W' nrs='0.18u / W'
+ sa=0 sb=0 sd=0 m=1
XMpref_dumm_TP[4] VDD VDD VDD VDD pfet_05v0 L=0.6u W=3.2u nf=1 ad='int((nf+1)/2) * W/nf * 0.18u' as='int((nf+2)/2) * W/nf * 0.18u'
+ pd='2*int((nf+1)/2) * (W/nf + 0.18u)' ps='2*int((nf+2)/2) * (W/nf + 0.18u)' nrd='0.18u / W' nrs='0.18u / W'
+ sa=0 sb=0 sd=0 m=1
XMpref_dumm_TP[3] VDD VDD VDD VDD pfet_05v0 L=0.6u W=3.2u nf=1 ad='int((nf+1)/2) * W/nf * 0.18u' as='int((nf+2)/2) * W/nf * 0.18u'
+ pd='2*int((nf+1)/2) * (W/nf + 0.18u)' ps='2*int((nf+2)/2) * (W/nf + 0.18u)' nrd='0.18u / W' nrs='0.18u / W'
+ sa=0 sb=0 sd=0 m=1
XMpref_dumm_TP[2] VDD VDD VDD VDD pfet_05v0 L=0.6u W=3.2u nf=1 ad='int((nf+1)/2) * W/nf * 0.18u' as='int((nf+2)/2) * W/nf * 0.18u'
+ pd='2*int((nf+1)/2) * (W/nf + 0.18u)' ps='2*int((nf+2)/2) * (W/nf + 0.18u)' nrd='0.18u / W' nrs='0.18u / W'
+ sa=0 sb=0 sd=0 m=1
XMpref_dumm_TP[1] VDD VDD VDD VDD pfet_05v0 L=0.6u W=3.2u nf=1 ad='int((nf+1)/2) * W/nf * 0.18u' as='int((nf+2)/2) * W/nf * 0.18u'
+ pd='2*int((nf+1)/2) * (W/nf + 0.18u)' ps='2*int((nf+2)/2) * (W/nf + 0.18u)' nrd='0.18u / W' nrs='0.18u / W'
+ sa=0 sb=0 sd=0 m=1
XMpref_dumm_TP[0] VDD VDD VDD VDD pfet_05v0 L=0.6u W=3.2u nf=1 ad='int((nf+1)/2) * W/nf * 0.18u' as='int((nf+2)/2) * W/nf * 0.18u'
+ pd='2*int((nf+1)/2) * (W/nf + 0.18u)' ps='2*int((nf+2)/2) * (W/nf + 0.18u)' nrd='0.18u / W' nrs='0.18u / W'
+ sa=0 sb=0 sd=0 m=1
**.ends
.end
